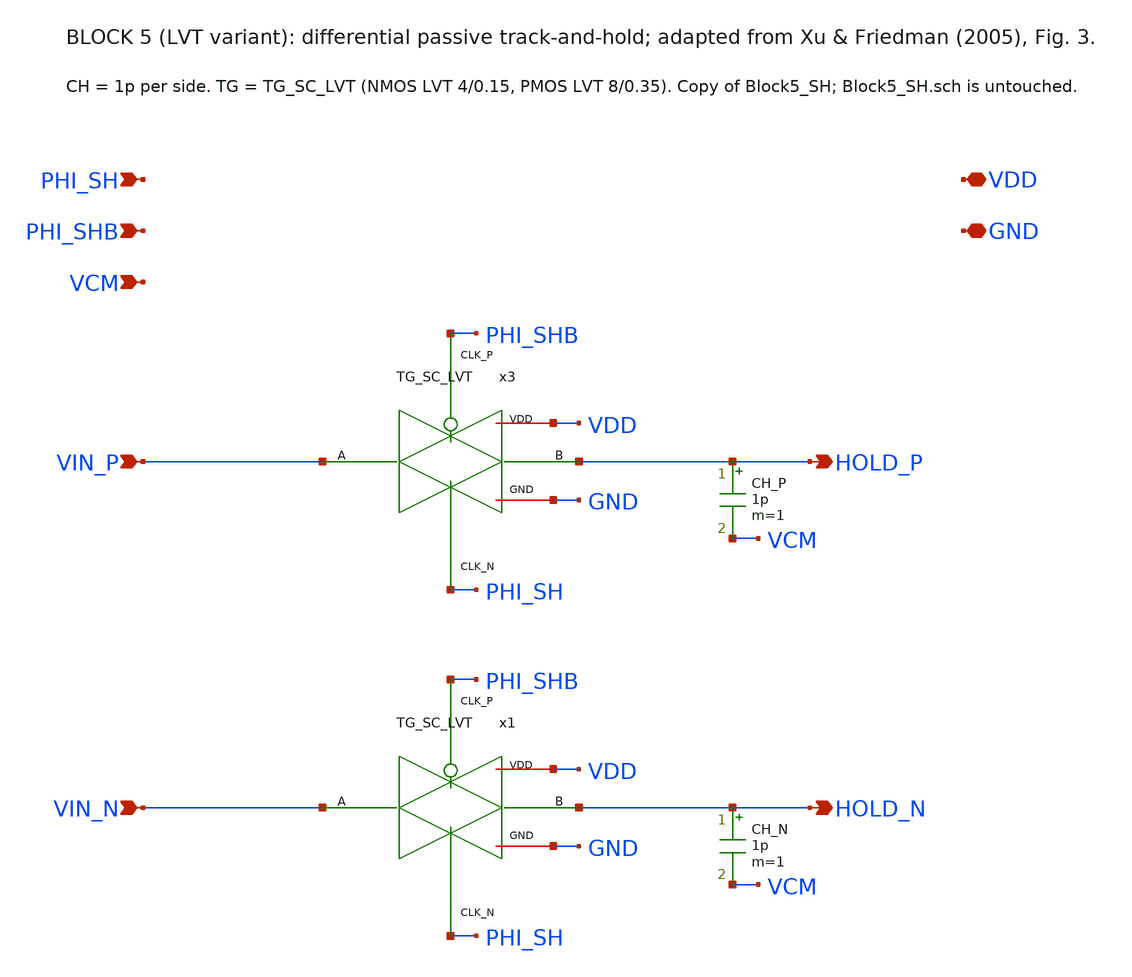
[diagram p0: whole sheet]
** sch_path: blocks/05_Switch_Network/xschem/Block5_SH_LVT.sch
**.subckt Block5_SH_LVT VIN_P VIN_N PHI_SH PHI_SHB VDD GND VCM HOLD_P HOLD_N
*.ipin VIN_P
*.ipin VIN_N
*.ipin PHI_SH
*.ipin PHI_SHB
*.iopin VDD
*.iopin GND
*.ipin VCM
*.opin HOLD_P
*.opin HOLD_N
CH_P HOLD_P VCM 1p m=1
CH_N HOLD_N VCM 1p m=1
x3 VIN_P HOLD_P PHI_SHB PHI_SH VDD GND TG_SC_LVT
x1 VIN_N HOLD_N PHI_SHB PHI_SH VDD GND TG_SC_LVT
**.ends

* expanding   symbol:  blocks/05_Switch_Network/xschem/TG_SC_LVT.sym # of pins=6
** sym_path: blocks/05_Switch_Network/xschem/TG_SC_LVT.sym
** sch_path: blocks/05_Switch_Network/xschem/TG_SC_LVT.sch
.subckt TG_SC_LVT A B CLK_P CLK_N VDD GND
*.iopin A
*.iopin B
*.ipin CLK_P
*.ipin CLK_N
*.iopin VDD
*.iopin GND
XMP A CLK_P B VDD sky130_fd_pr__pfet_01v8_lvt L=0.35 W=8 nf=1 ad='int((1 + 1)/2) * 8 / 1 * 0.29' as='int((1 + 2)/2) * 8 / 1 * 0.29'
+ pd='2*int((1 + 1)/2) * (8 / 1 + 0.29)' ps='2*int((1 + 2)/2) * (8 / 1 + 0.29)' nrd='0.29 / 8 ' nrs='0.29 / 8 '
+ sa=0 sb=0 sd=0 mult=1
XMN A CLK_N B GND sky130_fd_pr__nfet_01v8_lvt L=0.15 W=4 nf=1 ad='int((1 + 1)/2) * 4 / 1 * 0.29' as='int((1 + 2)/2) * 4 / 1 * 0.29'
+ pd='2*int((1 + 1)/2) * (4 / 1 + 0.29)' ps='2*int((1 + 2)/2) * (4 / 1 + 0.29)' nrd='0.29 / 4 ' nrs='0.29 / 4 '
+ sa=0 sb=0 sd=0 mult=1
.ends

.end
